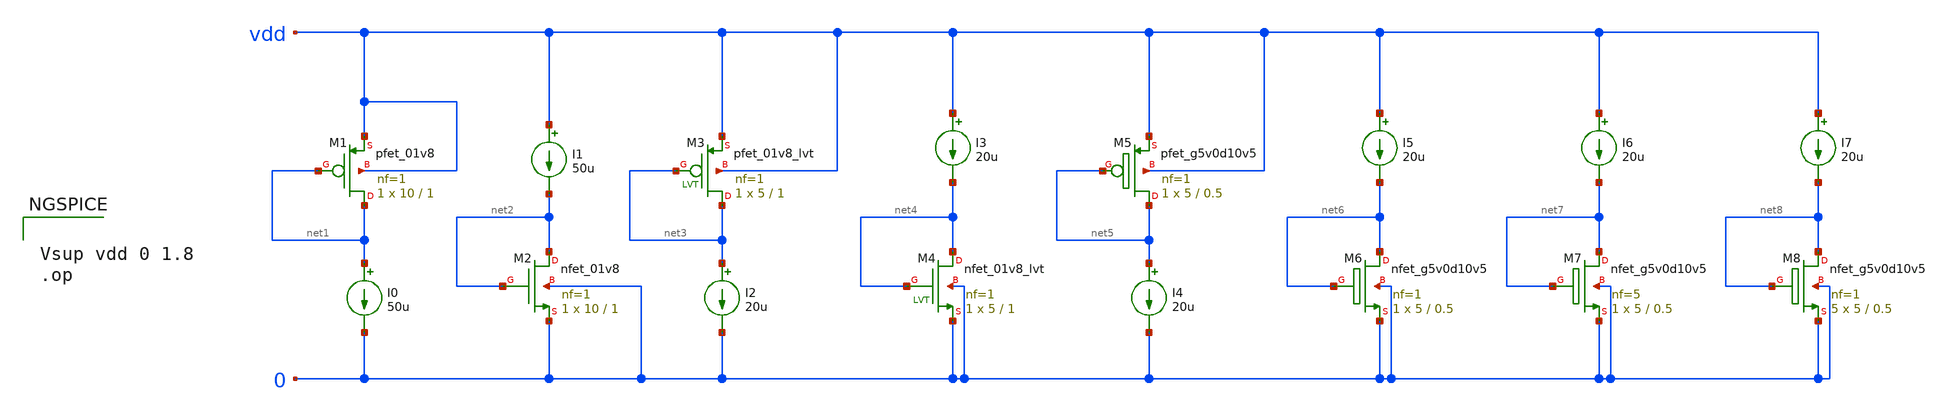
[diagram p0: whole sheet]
** sch_path: testing/test_mos.sch
**.subckt test_mos
XM1 net1 net1 vdd vdd sky130_fd_pr__pfet_01v8 L=1 W=10 nf=1 ad='int((nf+1)/2) * W/nf * 0.29' as='int((nf+2)/2) * W/nf * 0.29'
+ pd='2*int((nf+1)/2) * (W/nf + 0.29)' ps='2*int((nf+2)/2) * (W/nf + 0.29)' nrd='0.29 / W' nrs='0.29 / W'
+ sa=0 sb=0 sd=0 mult=1 m=1
I0 net1 0 50u
XM2 net2 net2 0 0 sky130_fd_pr__nfet_01v8 L=1 W=10 nf=1 ad='int((nf+1)/2) * W/nf * 0.29' as='int((nf+2)/2) * W/nf * 0.29'
+ pd='2*int((nf+1)/2) * (W/nf + 0.29)' ps='2*int((nf+2)/2) * (W/nf + 0.29)' nrd='0.29 / W' nrs='0.29 / W'
+ sa=0 sb=0 sd=0 mult=1 m=1
I1 vdd net2 50u
XM3 net3 net3 vdd vdd sky130_fd_pr__pfet_01v8_lvt L=1 W=5 nf=1 ad='int((nf+1)/2) * W/nf * 0.29' as='int((nf+2)/2) * W/nf * 0.29'
+ pd='2*int((nf+1)/2) * (W/nf + 0.29)' ps='2*int((nf+2)/2) * (W/nf + 0.29)' nrd='0.29 / W' nrs='0.29 / W'
+ sa=0 sb=0 sd=0 mult=1 m=1
I2 net3 0 20u
I3 vdd net4 20u
I4 net5 0 20u
I5 vdd net6 20u
XM4 net4 net4 0 0 sky130_fd_pr__nfet_01v8_lvt L=1 W=5 nf=1 ad='int((nf+1)/2) * W/nf * 0.29' as='int((nf+2)/2) * W/nf * 0.29'
+ pd='2*int((nf+1)/2) * (W/nf + 0.29)' ps='2*int((nf+2)/2) * (W/nf + 0.29)' nrd='0.29 / W' nrs='0.29 / W'
+ sa=0 sb=0 sd=0 mult=1 m=1
XM5 net5 net5 vdd vdd sky130_fd_pr__pfet_g5v0d10v5 L=0.5 W=5 nf=1 ad='int((nf+1)/2) * W/nf * 0.29' as='int((nf+2)/2) * W/nf * 0.29'
+ pd='2*int((nf+1)/2) * (W/nf + 0.29)' ps='2*int((nf+2)/2) * (W/nf + 0.29)' nrd='0.29 / W' nrs='0.29 / W'
+ sa=0 sb=0 sd=0 mult=1 m=1
XM6 net6 net6 0 0 sky130_fd_pr__nfet_g5v0d10v5 L=0.5 W=5 nf=1 ad='int((nf+1)/2) * W/nf * 0.29' as='int((nf+2)/2) * W/nf * 0.29'
+ pd='2*int((nf+1)/2) * (W/nf + 0.29)' ps='2*int((nf+2)/2) * (W/nf + 0.29)' nrd='0.29 / W' nrs='0.29 / W'
+ sa=0 sb=0 sd=0 mult=1 m=1
I6 vdd net7 20u
XM7 net7 net7 0 0 sky130_fd_pr__nfet_g5v0d10v5 L=0.5 W=5 nf=5 ad='int((nf+1)/2) * W/nf * 0.29' as='int((nf+2)/2) * W/nf * 0.29'
+ pd='2*int((nf+1)/2) * (W/nf + 0.29)' ps='2*int((nf+2)/2) * (W/nf + 0.29)' nrd='0.29 / W' nrs='0.29 / W'
+ sa=0 sb=0 sd=0 mult=1 m=1
I7 vdd net8 20u
XM8 net8 net8 0 0 sky130_fd_pr__nfet_g5v0d10v5 L=0.5 W=5 nf=1 ad='int((nf+1)/2) * W/nf * 0.29' as='int((nf+2)/2) * W/nf * 0.29'
+ pd='2*int((nf+1)/2) * (W/nf + 0.29)' ps='2*int((nf+2)/2) * (W/nf + 0.29)' nrd='0.29 / W' nrs='0.29 / W'
+ sa=0 sb=0 sd=0 mult=5 m=5
**** begin user architecture code

.include $::SKYWATER_MODELS/cells/nfet_01v8/sky130_fd_pr__nfet_01v8__tt.corner.spice
.include $::SKYWATER_MODELS/cells/nfet_01v8_lvt/sky130_fd_pr__nfet_01v8_lvt__tt.corner.spice
.include $::SKYWATER_MODELS/cells/pfet_01v8/sky130_fd_pr__pfet_01v8__tt.corner.spice
.include $::SKYWATER_MODELS/cells/nfet_03v3_nvt/sky130_fd_pr__nfet_03v3_nvt__tt.corner.spice
.include $::SKYWATER_MODELS/cells/nfet_05v0_nvt/sky130_fd_pr__nfet_05v0_nvt__tt.corner.spice
.include $::SKYWATER_MODELS/cells/esd_nfet_01v8/sky130_fd_pr__esd_nfet_01v8__tt.corner.spice
.include $::SKYWATER_MODELS/cells/pfet_01v8_lvt/sky130_fd_pr__pfet_01v8_lvt__tt.corner.spice
.include $::SKYWATER_MODELS/cells/pfet_01v8_hvt/sky130_fd_pr__pfet_01v8_hvt__tt.corner.spice
.include $::SKYWATER_MODELS/cells/esd_pfet_g5v0d10v5/sky130_fd_pr__esd_pfet_g5v0d10v5__tt.corner.spice
.include $::SKYWATER_MODELS/cells/pfet_g5v0d10v5/sky130_fd_pr__pfet_g5v0d10v5__tt.corner.spice
.include $::SKYWATER_MODELS/cells/pfet_g5v0d16v0/sky130_fd_pr__pfet_g5v0d16v0__tt.corner.spice
.include $::SKYWATER_MODELS/cells/nfet_g5v0d10v5/sky130_fd_pr__nfet_g5v0d10v5__tt.corner.spice
.include $::SKYWATER_MODELS/cells/nfet_g5v0d16v0/sky130_fd_pr__nfet_g5v0d16v0__tt_discrete.corner.spice
.include $::SKYWATER_MODELS/cells/esd_nfet_g5v0d10v5/sky130_fd_pr__esd_nfet_g5v0d10v5__tt.corner.spice
.include $::SKYWATER_MODELS/models/corners/tt/nonfet.spice
* Mismatch parameters
.include $::SKYWATER_MODELS/cells/nfet_01v8/sky130_fd_pr__nfet_01v8__mismatch.corner.spice
.include $::SKYWATER_MODELS/cells/pfet_01v8/sky130_fd_pr__pfet_01v8__mismatch.corner.spice
.include $::SKYWATER_MODELS/cells/nfet_01v8_lvt/sky130_fd_pr__nfet_01v8_lvt__mismatch.corner.spice
.include $::SKYWATER_MODELS/cells/pfet_01v8_lvt/sky130_fd_pr__pfet_01v8_lvt__mismatch.corner.spice
.include $::SKYWATER_MODELS/cells/pfet_01v8_hvt/sky130_fd_pr__pfet_01v8_hvt__mismatch.corner.spice
.include $::SKYWATER_MODELS/cells/nfet_g5v0d10v5/sky130_fd_pr__nfet_g5v0d10v5__mismatch.corner.spice
.include $::SKYWATER_MODELS/cells/pfet_g5v0d10v5/sky130_fd_pr__pfet_g5v0d10v5__mismatch.corner.spice
.include $::SKYWATER_MODELS/cells/nfet_05v0_nvt/sky130_fd_pr__nfet_05v0_nvt__mismatch.corner.spice
.include $::SKYWATER_MODELS/cells/nfet_03v3_nvt/sky130_fd_pr__nfet_03v3_nvt__mismatch.corner.spice
* Resistor$::SKYWATER_MODELS/Capacitor
.include $::SKYWATER_MODELS/models/r+c/res_typical__cap_typical.spice
.include $::SKYWATER_MODELS/models/r+c/res_typical__cap_typical__lin.spice
* Special cells
.include $::SKYWATER_MODELS/models/corners/tt/specialized_cells.spice
* All models
.include $::SKYWATER_MODELS/models/all.spice
* Corner
.include $::SKYWATER_MODELS/models/corners/tt/rf.spice



Vsup vdd 0 1.8
.op


**** end user architecture code
**.ends
.end
